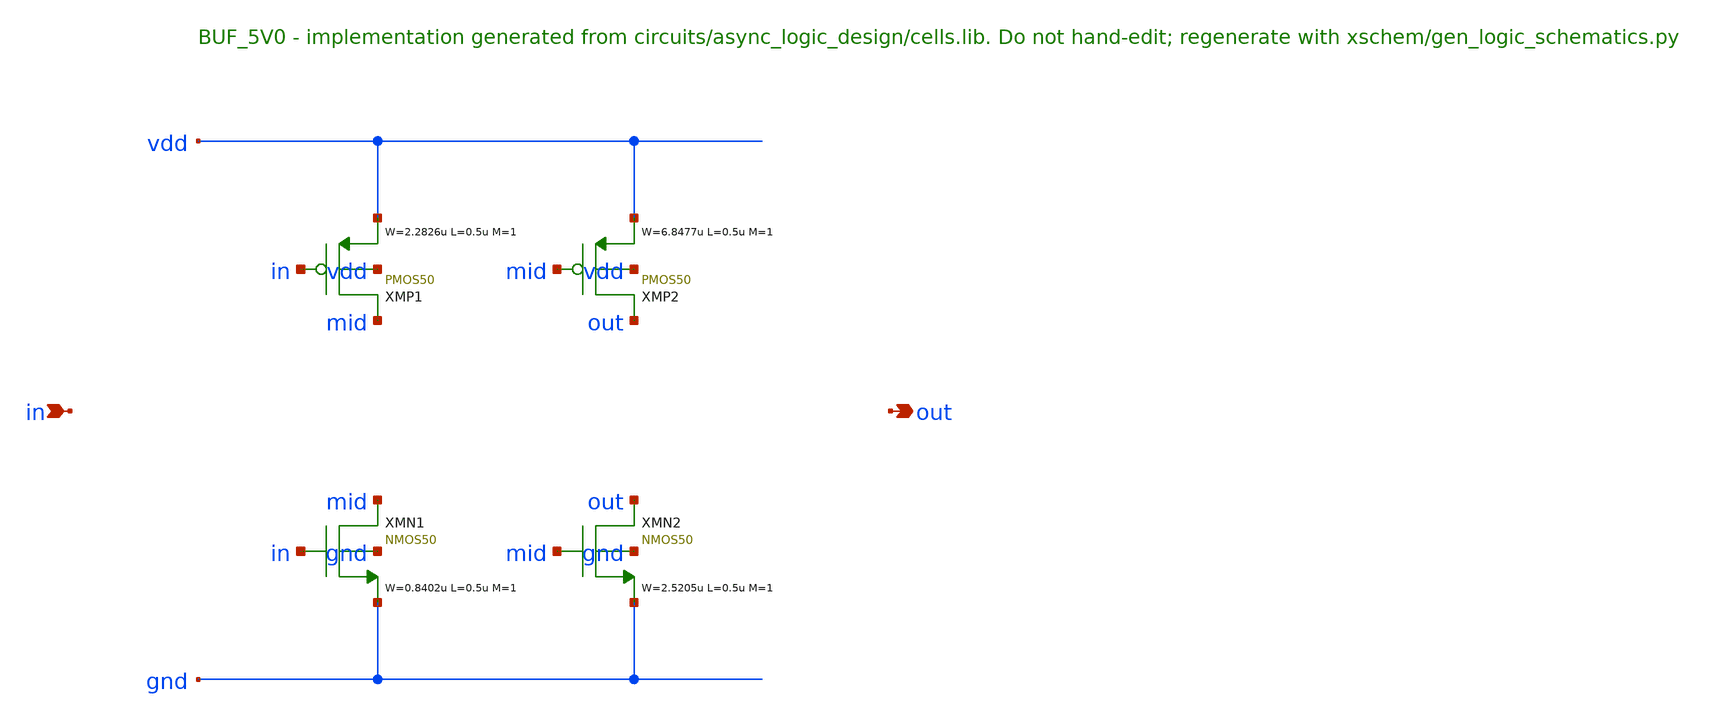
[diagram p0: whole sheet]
** sch_path: xschem/logic/BUF_5V0.sch
**.subckt BUF_5V0 in out
*.ipin in
*.opin out
XMP1 mid in vdd vdd PMOS50 W=2.2826u L=0.5u M=1 MM_SIGMA=0
XMP2 out mid vdd vdd PMOS50 W=6.8477u L=0.5u M=1 MM_SIGMA=0
XMN1 mid in gnd gnd NMOS50 W=0.8402u L=0.5u M=1 MM_SIGMA=0
XMN2 out mid gnd gnd NMOS50 W=2.5205u L=0.5u M=1 MM_SIGMA=0
**.ends
.end
